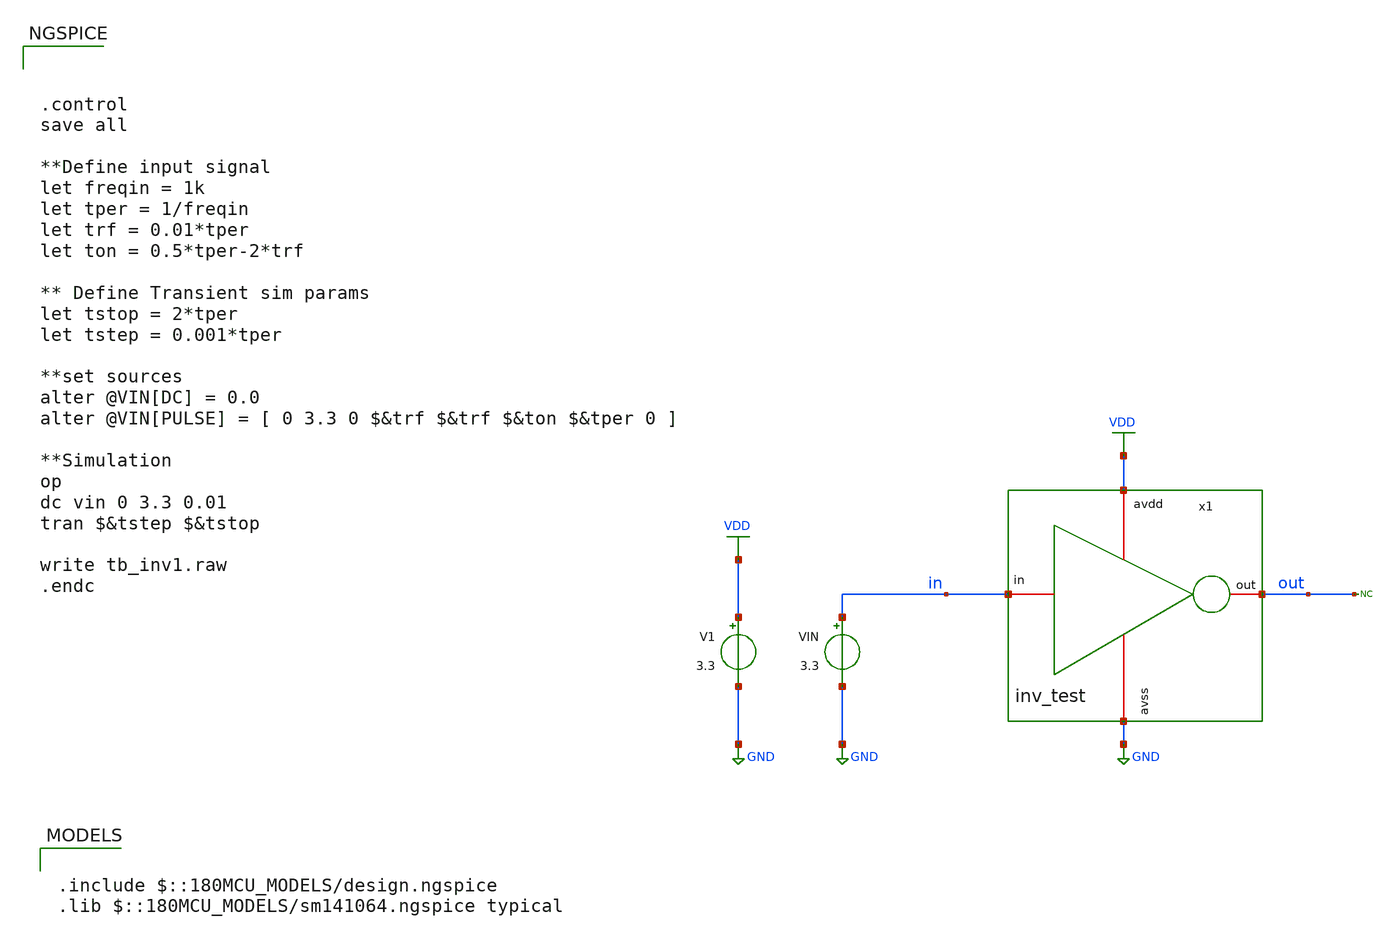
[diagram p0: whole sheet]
** sch_path: designs/libs/wk_kadam/tb_inv1.sch
**.subckt tb_inv1
x1 VDD in out GND inv_test
V1 VDD GND 3.3
VIN in GND 3.3
* noconn out
**** begin user architecture code

.include $::180MCU_MODELS/design.ngspice
.lib $::180MCU_MODELS/sm141064.ngspice typical




.control
save all

**Define input signal
let freqin = 1k
let tper = 1/freqin
let trf = 0.01*tper
let ton = 0.5*tper-2*trf

** Define Transient sim params
let tstop = 2*tper
let tstep = 0.001*tper

**set sources
alter @VIN[DC] = 0.0
alter @VIN[PULSE] = [ 0 3.3 0 $&trf $&trf $&ton $&tper 0 ]

**Simulation
op
dc vin 0 3.3 0.01
tran $&tstep $&tstop

write tb_inv1.raw
.endc


**** end user architecture code
**.ends

* expanding   symbol:  libs/wk_kadam/inv_test.sym # of pins=4
** sym_path: designs/libs/wk_kadam/inv_test.sym
** sch_path: designs/libs/wk_kadam/inv_test.sch
.subckt inv_test avdd in out avss
*.iopin avdd
*.iopin avss
*.iopin in
*.iopin out
XM3 out in avss avss nfet_03v3 L=0.28u W=1.0u nf=1 ad='int((nf+1)/2) * W/nf * 0.18u' as='int((nf+2)/2) * W/nf * 0.18u'
+ pd='2*int((nf+1)/2) * (W/nf + 0.18u)' ps='2*int((nf+2)/2) * (W/nf + 0.18u)' nrd='0.18u / W' nrs='0.18u / W'
+ sa=0 sb=0 sd=0 m=1
XM4 out in avdd avdd pfet_03v3 L=0.28u W=2.0u nf=1 ad='int((nf+1)/2) * W/nf * 0.18u' as='int((nf+2)/2) * W/nf * 0.18u'
+ pd='2*int((nf+1)/2) * (W/nf + 0.18u)' ps='2*int((nf+2)/2) * (W/nf + 0.18u)' nrd='0.18u / W' nrs='0.18u / W'
+ sa=0 sb=0 sd=0 m=1
.ends

.GLOBAL VDD
.GLOBAL GND
.end
